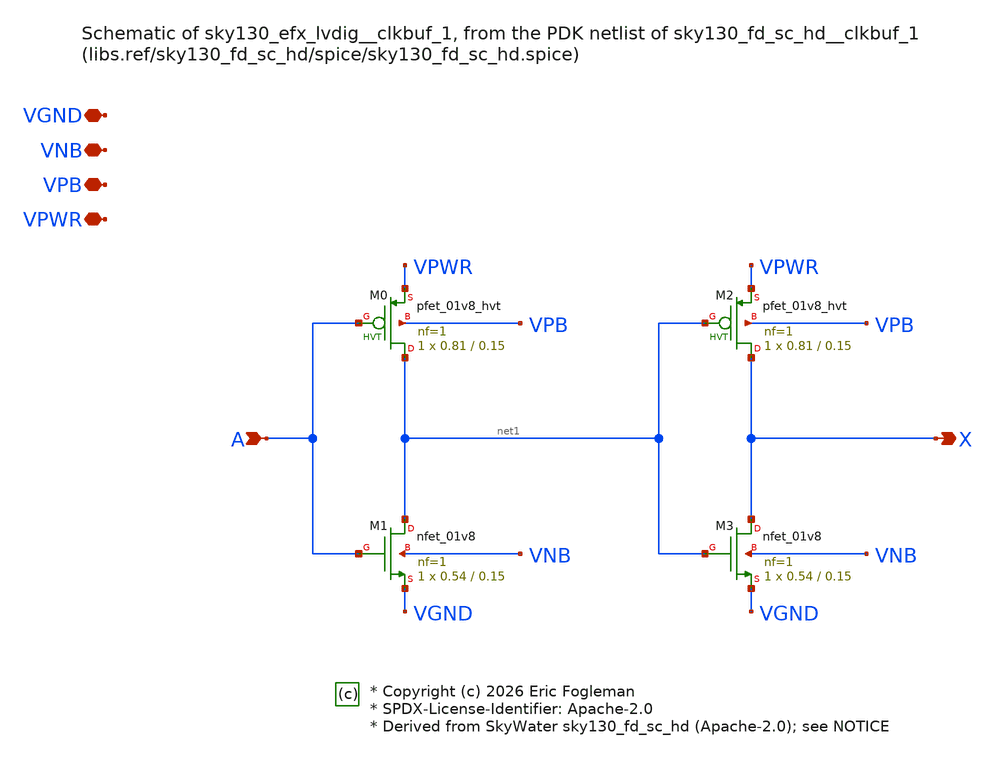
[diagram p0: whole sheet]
** sch_path: xschem/sky130_efx_lvdig__clkbuf_1.sch

* Copyright (c) 2026 Eric Fogleman
* SPDX-License-Identifier: Apache-2.0
* Derived from SkyWater sky130_fd_sc_hd (Apache-2.0); see NOTICE

**.subckt sky130_efx_lvdig__clkbuf_1 A X VGND VNB VPB VPWR
*.ipin A
*.opin X
*.iopin VGND
*.iopin VNB
*.iopin VPB
*.iopin VPWR
XM0 net1 A VPWR VPB sky130_fd_pr__pfet_01v8_hvt L=0.15 W=0.81 nf=1 ad='int((1 + 1)/2) * 0.81 / 1 * 0.29'
+ as='int((1 + 2)/2) * 0.81 / 1 * 0.29' pd='2*int((1 + 1)/2) * (0.81 / 1 + 0.29)' ps='2*int((1 + 2)/2) * (0.81 / 1 + 0.29)'
+ nrd='0.29 / 0.81 ' nrs='0.29 / 0.81 ' sa=0 sb=0 sd=0 mult=1 m=1
XM1 net1 A VGND VNB sky130_fd_pr__nfet_01v8 L=0.15 W=0.54 nf=1 ad='int((1 + 1)/2) * 0.54 / 1 * 0.29'
+ as='int((1 + 2)/2) * 0.54 / 1 * 0.29' pd='2*int((1 + 1)/2) * (0.54 / 1 + 0.29)' ps='2*int((1 + 2)/2) * (0.54 / 1 + 0.29)'
+ nrd='0.29 / 0.54 ' nrs='0.29 / 0.54 ' sa=0 sb=0 sd=0 mult=1 m=1
XM2 X net1 VPWR VPB sky130_fd_pr__pfet_01v8_hvt L=0.15 W=0.81 nf=1 ad='int((1 + 1)/2) * 0.81 / 1 * 0.29'
+ as='int((1 + 2)/2) * 0.81 / 1 * 0.29' pd='2*int((1 + 1)/2) * (0.81 / 1 + 0.29)' ps='2*int((1 + 2)/2) * (0.81 / 1 + 0.29)'
+ nrd='0.29 / 0.81 ' nrs='0.29 / 0.81 ' sa=0 sb=0 sd=0 mult=1 m=1
XM3 X net1 VGND VNB sky130_fd_pr__nfet_01v8 L=0.15 W=0.54 nf=1 ad='int((1 + 1)/2) * 0.54 / 1 * 0.29'
+ as='int((1 + 2)/2) * 0.54 / 1 * 0.29' pd='2*int((1 + 1)/2) * (0.54 / 1 + 0.29)' ps='2*int((1 + 2)/2) * (0.54 / 1 + 0.29)'
+ nrd='0.29 / 0.54 ' nrs='0.29 / 0.54 ' sa=0 sb=0 sd=0 mult=1 m=1
**.ends
.end
